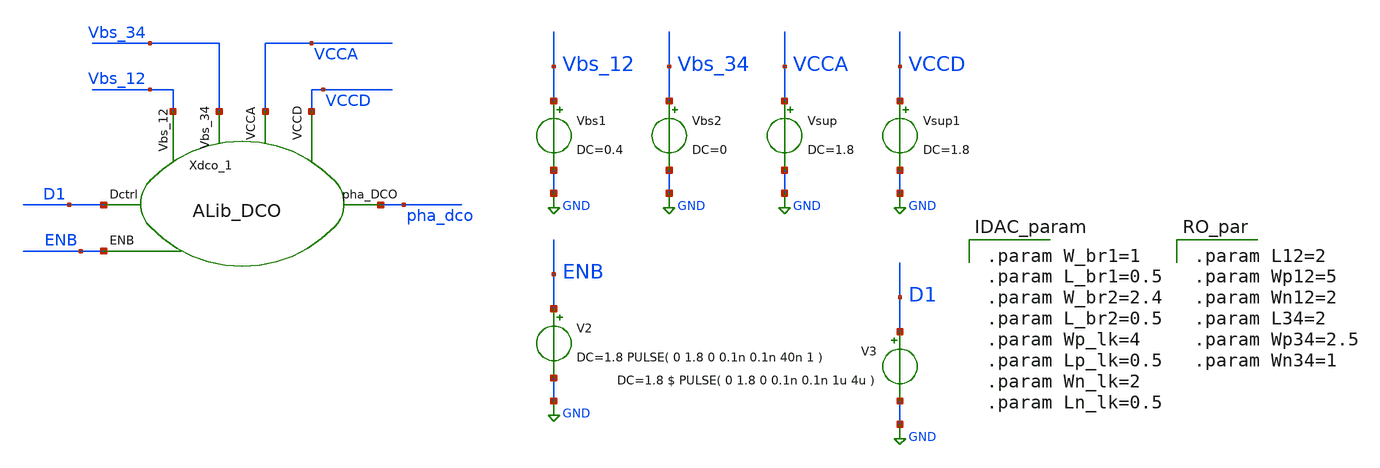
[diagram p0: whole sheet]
** sch_path: xschem/tb/DCO_tb.sch
**.subckt DCO_tb
Vsup VCCA GND DC=1.8
Vbs1 Vbs_12 GND DC=0.4
V2 ENB GND DC=1.8 PULSE( 0 1.8 0 0.1n 0.1n 40n 1 )
V3 D1 GND DC=1.8 $ PULSE( 0 1.8 0 0.1n 0.1n 1u 4u )
Vbs2 Vbs_34 GND DC=0
Vsup1 VCCD GND DC=1.8
Xdco_1 D1 ENB Vbs_12 Vbs_34 VCCD VCCA pha_dco ALib_DCO
**** begin user architecture code

.param W_br1=1
.param L_br1=0.5
.param W_br2=2.4
.param L_br2=0.5
.param Wp_lk=4
.param Lp_lk=0.5
.param Wn_lk=2
.param Ln_lk=0.5


.param L12=2
.param Wp12=5
.param Wn12=2
.param L34=2
.param Wp34=2.5
.param Wn34=1



** Library on VNU server
.lib /home/dkits/efabless/mpw-5/pdks/sky130A/libs.tech/ngspice/sky130.lib.spice tt
.inc /home/dkits/efabless/mpw-5/pdks/sky130A/libs.ref/sky130_fd_sc_hd/spice/sky130_fd_sc_hd.spice
** Library on Home PC
*.lib /home/dkit/efabless/pdks/sky130A/libs.tech/ngspice/sky130.lib.spice tt
*.inc /home/dkit/efabless/pdks/sky130A/libs.ref/sky130_fd_sc_hd/spice/sky130_fd_sc_hd.spice




.param mc_mm_switch=0
.control
set nobreak
set num_threads=6
set test_mode = 0
* mode = 0: operation testing    1:  frequency extraction    2:  power consumption
if ($test_mode = 0)
    TRAN 1n 5u
    plot pha_dco
    MEAS TRAN prd TRIG pha_dco VAL=0.8 RISE=10 TARG pha_dco VAL=0.8 RISE=20
    let freq = 10/prd
    echo "frequency: "
    print freq
end
if ($test_mode = 1)
    let Vlow = 0
    let Vlimit = 1.01     $ set upper bound for sweeping
    let Vsweep = 0.2      $ set step size for sweeping
    let NoPoints=(Vlimit-Vlow)/Vsweep+2    $ set number of points for sweeping
    let freq =unitvec(NoPoints)
    let Vin  =unitvec(NoPoints)
    let Vin[0]=Vlow
    let ix=0
    while Vin[ix] < Vlimit
        alter Vground DC=Vin[ix]
        TRAN 0.4n 12u
        MEAS TRAN prd TRIG pha_dco VAL=0.8 RISE=10 TARG pha_dco VAL=0.8 RISE =20
        let freq[ix] = 10/prd
        let ix = ix+1
        Let Vin[ix] = Vin[ix-1]+Vsweep
    end
   print Vin freq
end
if ($test_mode = 2)
    save vdd @Vsup[i] pha_dco
    TRAN 0.1n 5u
    MEAS TRAN I_vco AVG @Vsup[i] FROM=3u TO=4u
    MEAS TRAN V_vco AVG vdd FROM=3u TO=4u
    let Power=I_vco*V_vco
    print Power
end
.endc


**** end user architecture code
**.ends
.GLOBAL GND
.end
